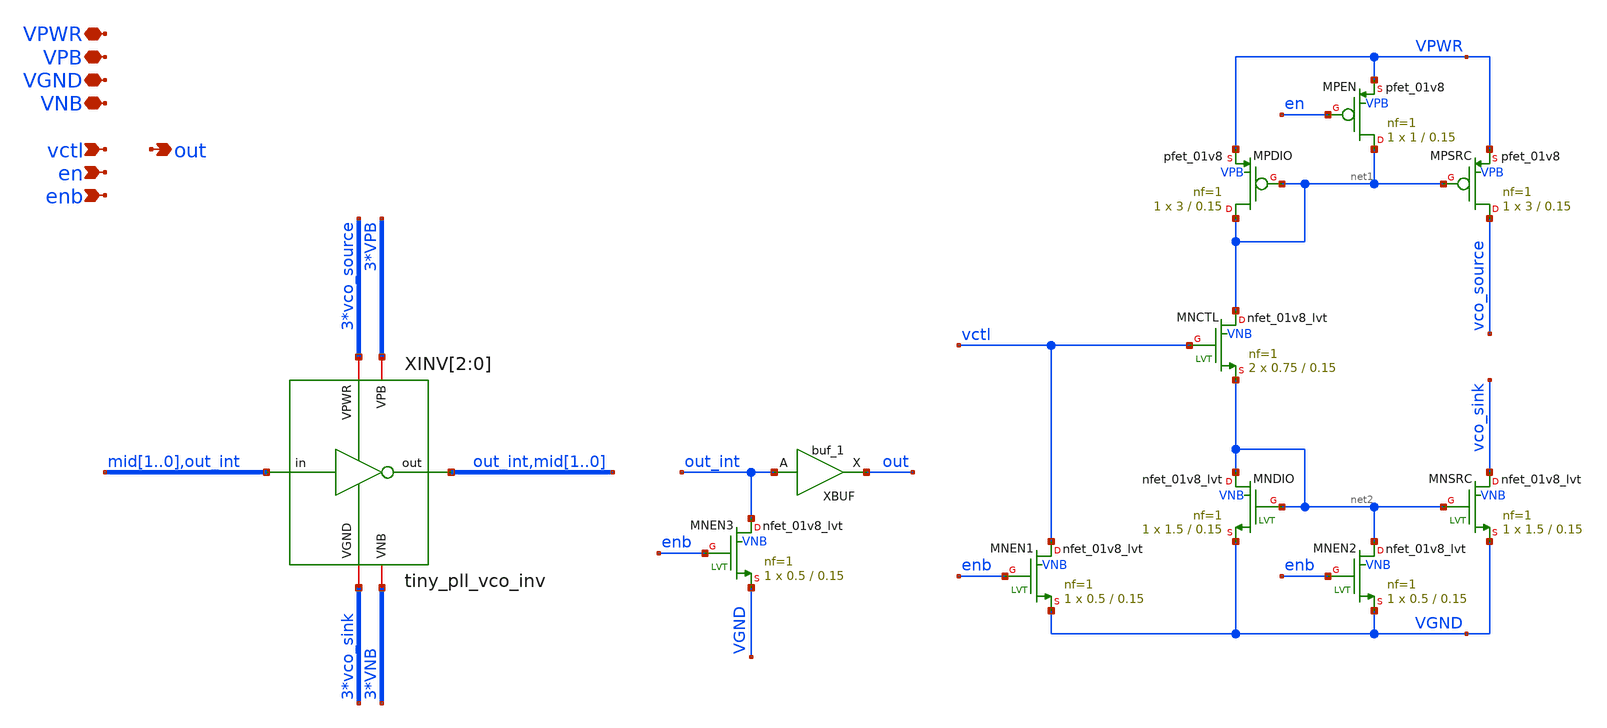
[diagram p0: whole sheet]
** sch_path: xschem/tiny_pll/tiny_pll_vco.sch
**.subckt tiny_pll_vco vctl out VPWR VPB VGND VNB en enb
*.ipin vctl
*.opin out
*.iopin VPWR
*.iopin VPB
*.iopin VGND
*.iopin VNB
*.ipin en
*.ipin enb
XINV[2] vco_source VPB vco_sink VNB out_int mid1 tiny_pll_vco_inv
XINV[1] vco_source VPB vco_sink VNB mid1 mid0 tiny_pll_vco_inv
XINV[0] vco_source VPB vco_sink VNB mid0 out_int tiny_pll_vco_inv
XMNDIO net2 net2 VGND VNB sky130_fd_pr__nfet_01v8_lvt L=0.15 W=1.5 nf=1 ad='int((nf+1)/2) * W/nf * 0.29'
+ as='int((nf+2)/2) * W/nf * 0.29' pd='2*int((nf+1)/2) * (W/nf + 0.29)' ps='2*int((nf+2)/2) * (W/nf + 0.29)'
+ nrd='0.29 / W' nrs='0.29 / W' sa=0 sb=0 sd=0 mult=1 m=1
XMNSRC vco_sink net2 VGND VNB sky130_fd_pr__nfet_01v8_lvt L=0.15 W=1.5 nf=1 ad='int((nf+1)/2) * W/nf * 0.29'
+ as='int((nf+2)/2) * W/nf * 0.29' pd='2*int((nf+1)/2) * (W/nf + 0.29)' ps='2*int((nf+2)/2) * (W/nf + 0.29)'
+ nrd='0.29 / W' nrs='0.29 / W' sa=0 sb=0 sd=0 mult=1 m=1
XMPDIO net1 net1 VPWR VPB sky130_fd_pr__pfet_01v8 L=0.15 W=3 nf=1 ad='int((nf+1)/2) * W/nf * 0.29' as='int((nf+2)/2) * W/nf * 0.29'
+ pd='2*int((nf+1)/2) * (W/nf + 0.29)' ps='2*int((nf+2)/2) * (W/nf + 0.29)' nrd='0.29 / W' nrs='0.29 / W'
+ sa=0 sb=0 sd=0 mult=1 m=1
XMPSRC vco_source net1 VPWR VPB sky130_fd_pr__pfet_01v8 L=0.15 W=3 nf=1 ad='int((nf+1)/2) * W/nf * 0.29'
+ as='int((nf+2)/2) * W/nf * 0.29' pd='2*int((nf+1)/2) * (W/nf + 0.29)' ps='2*int((nf+2)/2) * (W/nf + 0.29)'
+ nrd='0.29 / W' nrs='0.29 / W' sa=0 sb=0 sd=0 mult=1 m=1
XMNCTL net1 vctl net2 VNB sky130_fd_pr__nfet_01v8_lvt L=0.15 W=0.75 nf=1 ad='int((nf+1)/2) * W/nf * 0.29'
+ as='int((nf+2)/2) * W/nf * 0.29' pd='2*int((nf+1)/2) * (W/nf + 0.29)' ps='2*int((nf+2)/2) * (W/nf + 0.29)'
+ nrd='0.29 / W' nrs='0.29 / W' sa=0 sb=0 sd=0 mult=2 m=2
XBUF out_int VGND VNB VPB VPWR out sky130_fd_sc_hd__buf_1
XMNEN1 vctl enb VGND VNB sky130_fd_pr__nfet_01v8_lvt L=0.15 W=0.5 nf=1 ad='int((nf+1)/2) * W/nf * 0.29'
+ as='int((nf+2)/2) * W/nf * 0.29' pd='2*int((nf+1)/2) * (W/nf + 0.29)' ps='2*int((nf+2)/2) * (W/nf + 0.29)'
+ nrd='0.29 / W' nrs='0.29 / W' sa=0 sb=0 sd=0 mult=1 m=1
XMNEN2 net2 enb VGND VNB sky130_fd_pr__nfet_01v8_lvt L=0.15 W=0.5 nf=1 ad='int((nf+1)/2) * W/nf * 0.29'
+ as='int((nf+2)/2) * W/nf * 0.29' pd='2*int((nf+1)/2) * (W/nf + 0.29)' ps='2*int((nf+2)/2) * (W/nf + 0.29)'
+ nrd='0.29 / W' nrs='0.29 / W' sa=0 sb=0 sd=0 mult=1 m=1
XMPEN net1 en VPWR VPB sky130_fd_pr__pfet_01v8 L=0.15 W=1 nf=1 ad='int((nf+1)/2) * W/nf * 0.29' as='int((nf+2)/2) * W/nf * 0.29'
+ pd='2*int((nf+1)/2) * (W/nf + 0.29)' ps='2*int((nf+2)/2) * (W/nf + 0.29)' nrd='0.29 / W' nrs='0.29 / W'
+ sa=0 sb=0 sd=0 mult=1 m=1
XMNEN3 out_int enb VGND VNB sky130_fd_pr__nfet_01v8_lvt L=0.15 W=0.5 nf=1 ad='int((nf+1)/2) * W/nf * 0.29'
+ as='int((nf+2)/2) * W/nf * 0.29' pd='2*int((nf+1)/2) * (W/nf + 0.29)' ps='2*int((nf+2)/2) * (W/nf + 0.29)'
+ nrd='0.29 / W' nrs='0.29 / W' sa=0 sb=0 sd=0 mult=1 m=1
**.ends

* expanding   symbol:  tiny_pll_vco_inv.sym # of pins=6
** sym_path: xschem/tiny_pll/tiny_pll_vco_inv.sym
** sch_path: xschem/tiny_pll/tiny_pll_vco_inv.sch
.subckt tiny_pll_vco_inv VPWR VPB VGND VNB out in
*.ipin in
*.opin out
*.iopin VPWR
*.iopin VPB
*.iopin VGND
*.iopin VNB
x1 in VGND VNB VPB VPWR out sky130_fd_sc_hd__inv_1
.ends

.end
